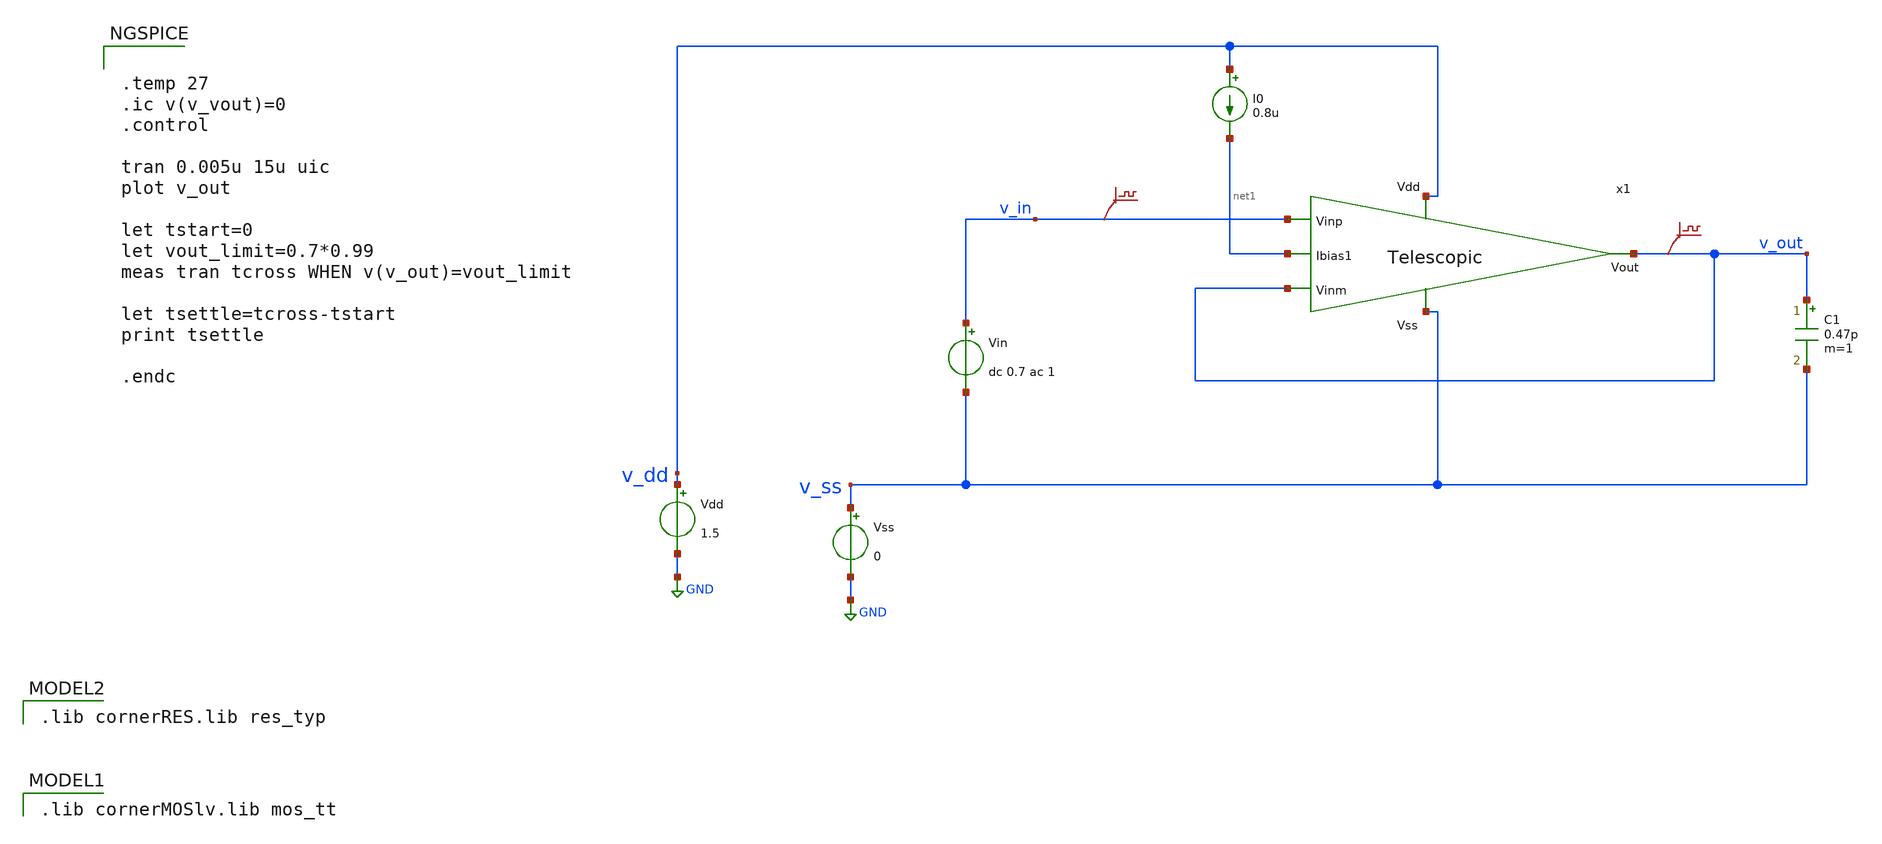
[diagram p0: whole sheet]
** sch_path: DSM/Schematics/Designs_Hrishi/RealCircuits/Telescopic/tb_Telescopic_tran.sch
* (c) 2024 Hrishikesh, @HSB
**.subckt tb_Telescopic_tran
Vss v_ss GND 0
Vdd v_dd GND 1.5
Vin v_in v_ss dc 0.7 ac 1
.save v(v_in)
I0 v_dd net1 0.8u
C1 v_out v_ss 0.47p m=1
.save v(v_out)
x1 v_dd net1 v_out v_out v_in v_ss Telescopic
**** begin user architecture code
 .lib cornerMOSlv.lib mos_tt

 .lib cornerRES.lib res_typ



.temp 27
.ic v(v_vout)=0
.control

tran 0.005u 15u uic
plot v_out

let tstart=0
let vout_limit=0.7*0.99
meas tran tcross WHEN v(v_out)=vout_limit

let tsettle=tcross-tstart
print tsettle

.endc


**** end user architecture code
**.ends

* expanding   symbol:
*+  /foss/designs/CEMS_DSM/DSM/Schematics/Designs_Hrishi/RealCircuits/Telescopic/Telescopic.sym # of pins=6
** sym_path: DSM/IC_Designs_Hrishi/RealCircuits/Telescopic/Telescopic.sym
** sch_path: DSM/IC_Designs_Hrishi/RealCircuits/Telescopic/Telescopic.sch
.subckt Telescopic Vdd Ibias1 Vout Vinm Vinp Vss
*.ipin Vinp
*.opin Vout
*.ipin Vinm
*.ipin Vss
*.ipin Vdd
*.ipin Ibias1
XM19 net1 net8 Vss Vss sg13_lv_nmos w=0.272u l=0.2u ng=1 m=1 mm_ok=1
XM11 net2 Vinp net1 Vss sg13_lv_nmos w=0.13u l=0.6u ng=1 m=1 mm_ok=1
XM26 Ibias1 Ibias1 net8 Vss sg13_lv_nmos w=0.13u l=0.6u ng=1 m=1 mm_ok=1
XM27 net8 net8 Vss Vss sg13_lv_nmos w=0.13u l=0.6u ng=1 m=1 mm_ok=1
XM28 net6 net8 Vss Vss sg13_lv_nmos w=0.13u l=0.6u ng=1 m=1 mm_ok=1
XM23 Vout Ibias1 net3 Vss sg13_lv_nmos w=0.13u l=0.6u ng=1 m=1 mm_ok=1
XM14 net3 Vinm net1 Vss sg13_lv_nmos w=0.13u l=0.6u ng=1 m=1 mm_ok=1
XM22 net7 Ibias1 net2 Vss sg13_lv_nmos w=0.13u l=0.6u ng=1 m=1 mm_ok=1
XM29 net7 net7 Vdd Vdd sg13_lv_pmos w=0.375u l=0.4u ng=1 m=1 mm_ok=1
XM30 net6 net6 net7 Vdd sg13_lv_pmos w=0.375u l=0.4u ng=1 m=1 mm_ok=1
XM20 Vout net6 net5 Vdd sg13_lv_pmos w=0.375u l=0.4u ng=1 m=1 mm_ok=1
XM24 net5 net7 Vdd Vdd sg13_lv_pmos w=0.375u l=0.4u ng=1 m=1 mm_ok=1
XM21 net4 net7 Vdd Vdd sg13_lv_pmos w=0.375u l=0.4u ng=1 m=1 mm_ok=1
XM25 net7 net6 net4 Vdd sg13_lv_pmos w=0.375u l=0.4u ng=1 m=1 mm_ok=1
.ends

.GLOBAL GND
.end
